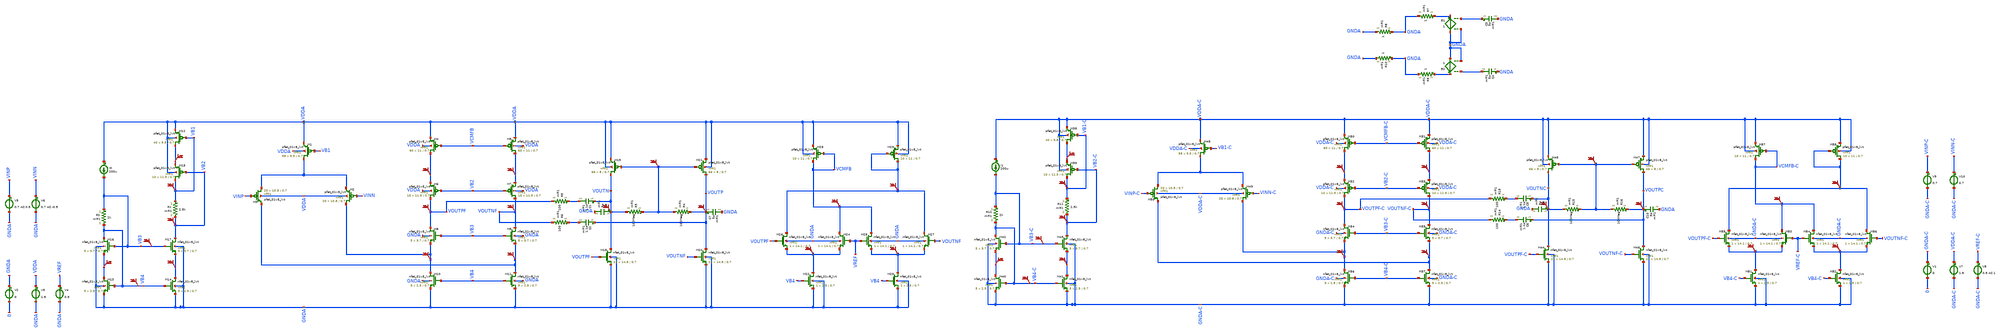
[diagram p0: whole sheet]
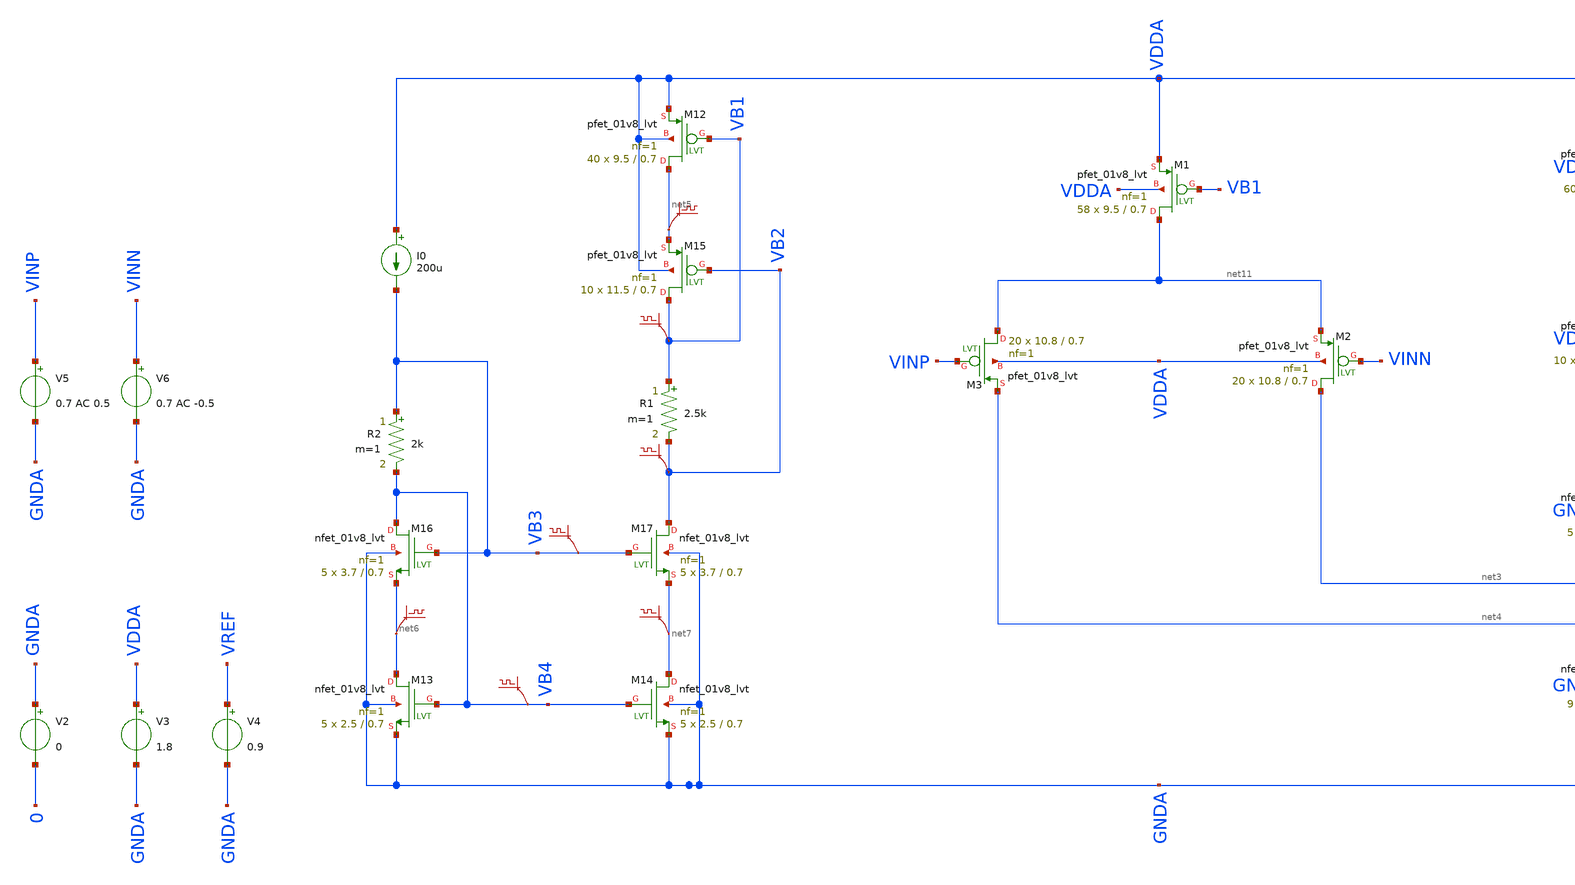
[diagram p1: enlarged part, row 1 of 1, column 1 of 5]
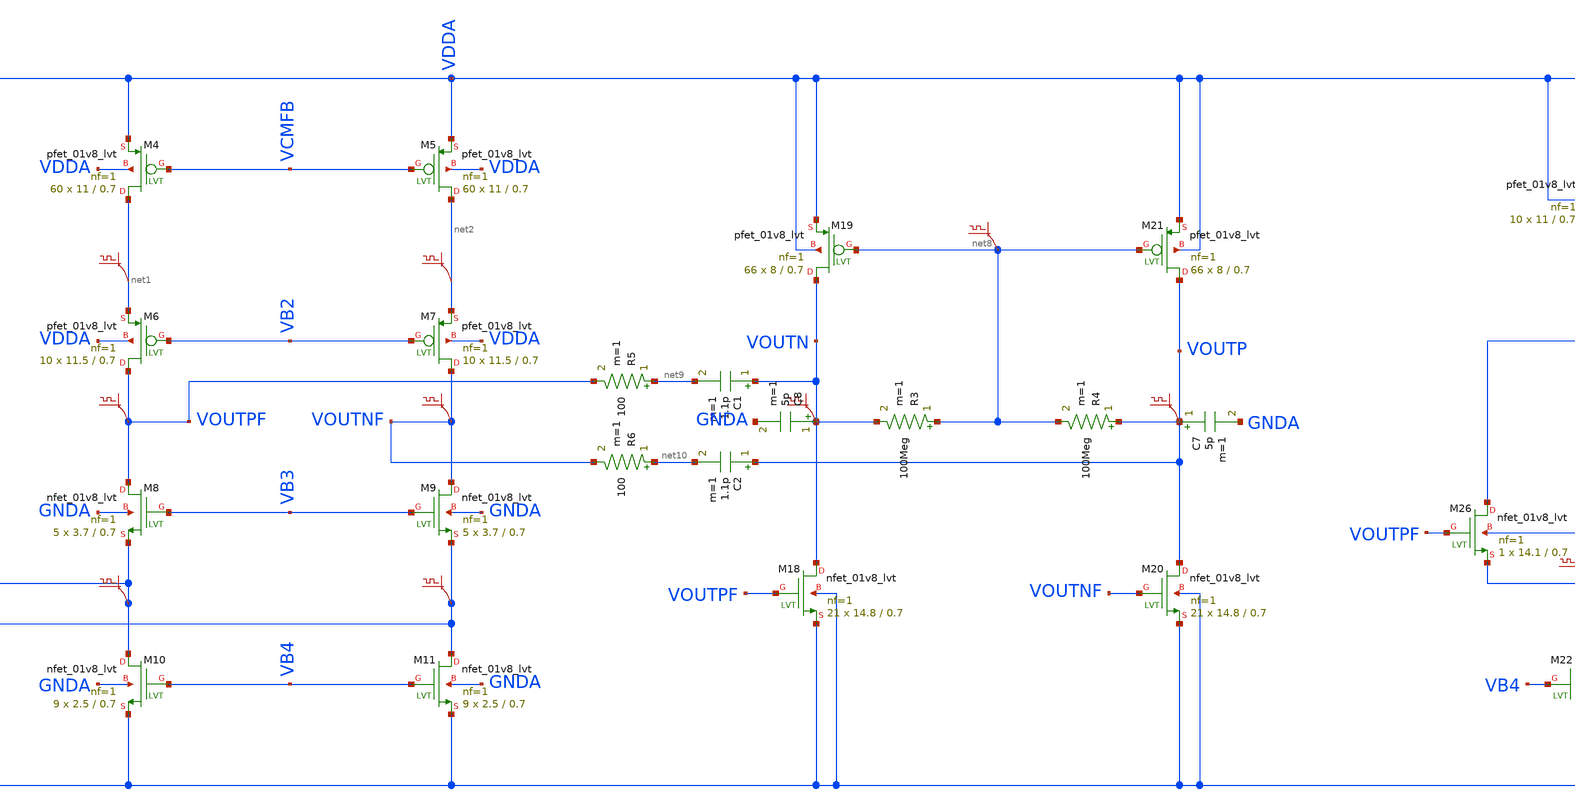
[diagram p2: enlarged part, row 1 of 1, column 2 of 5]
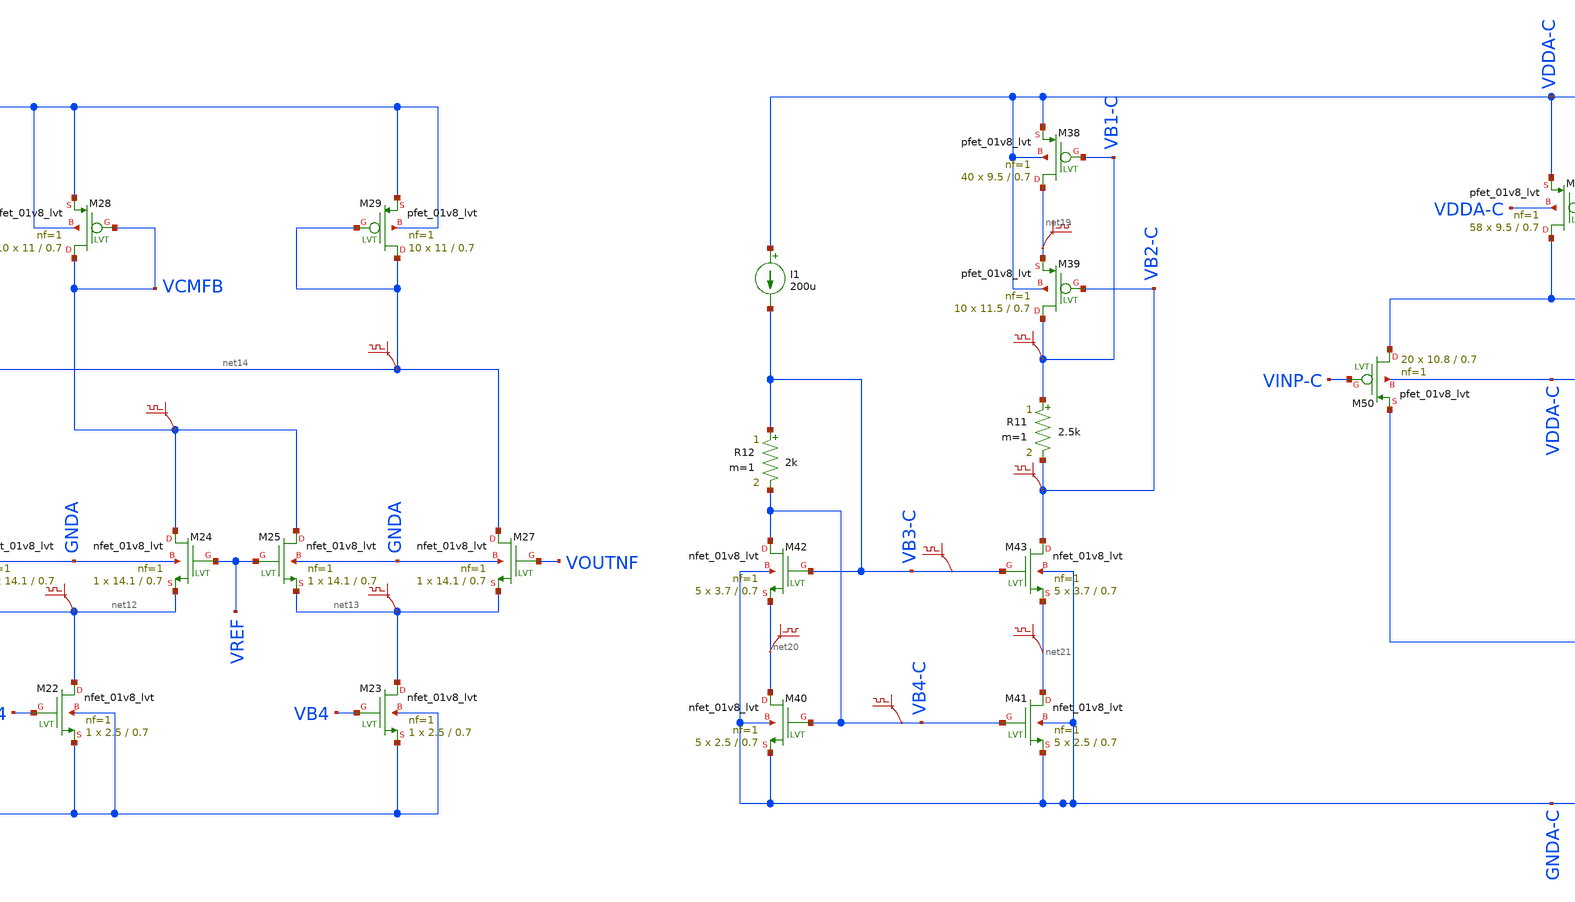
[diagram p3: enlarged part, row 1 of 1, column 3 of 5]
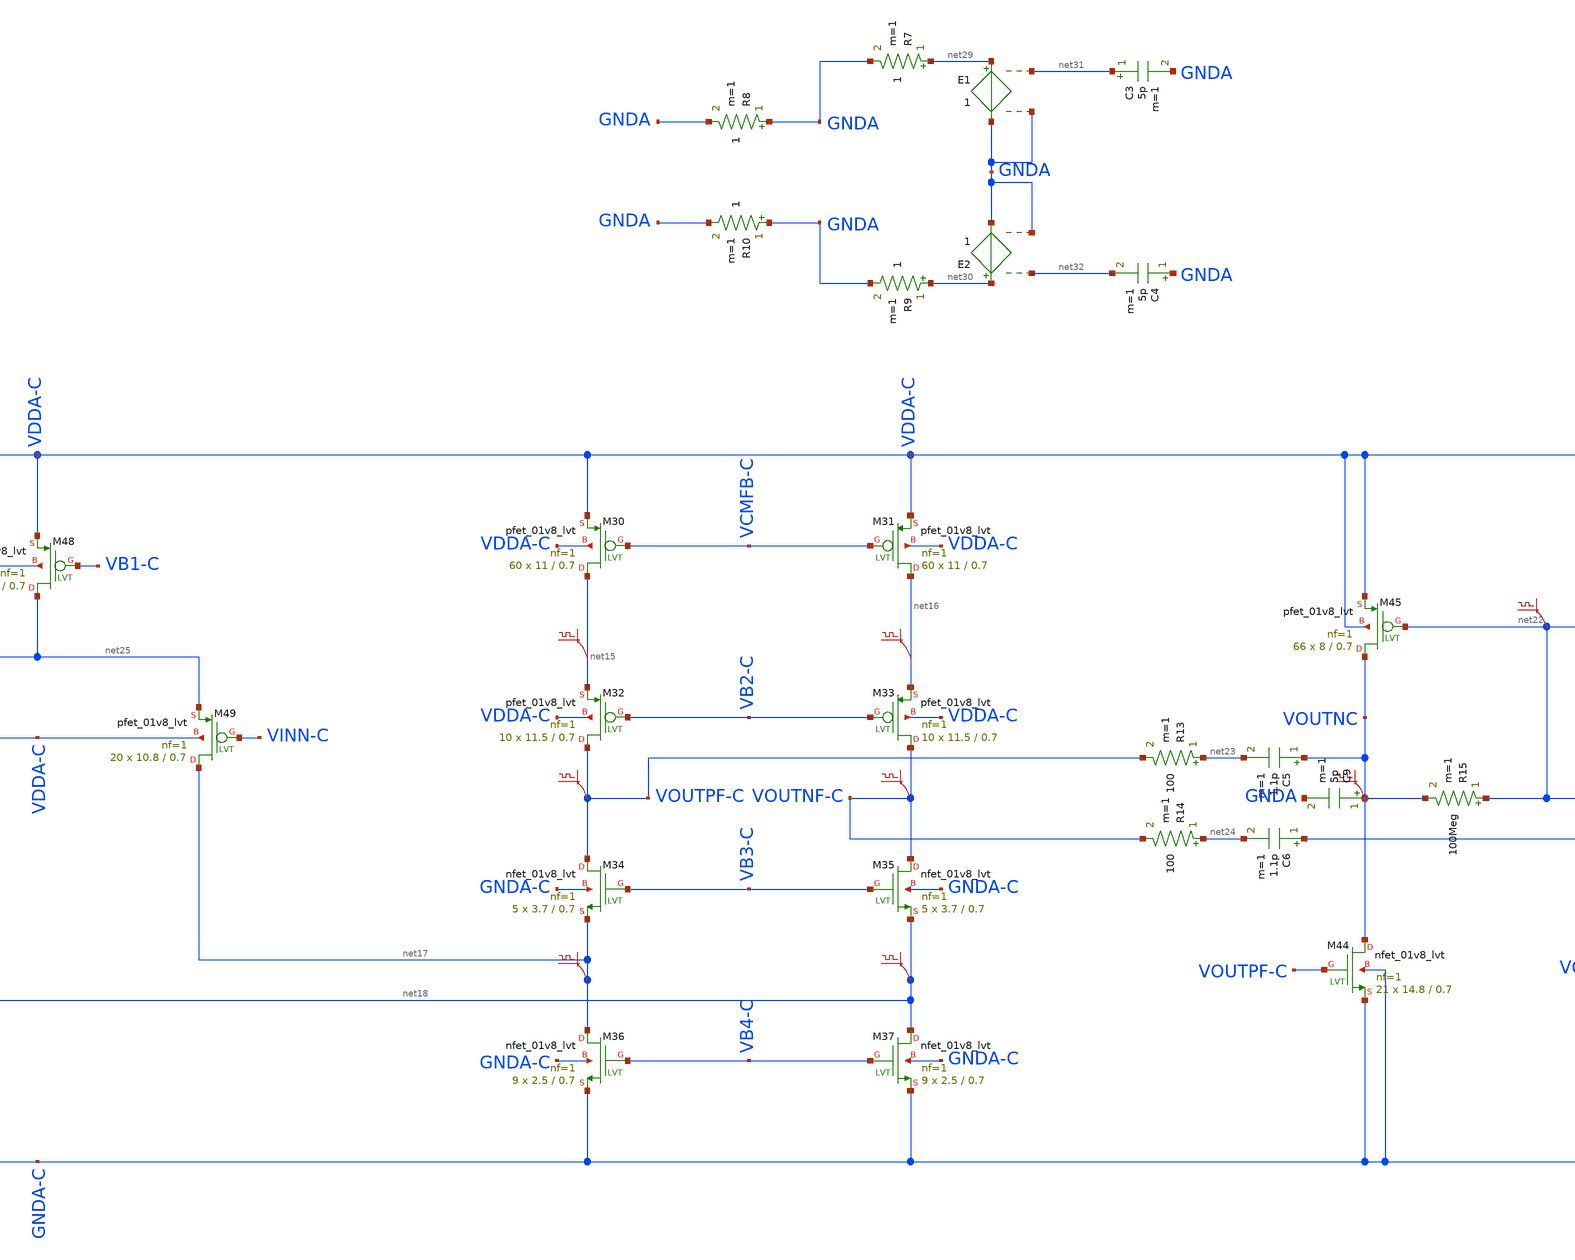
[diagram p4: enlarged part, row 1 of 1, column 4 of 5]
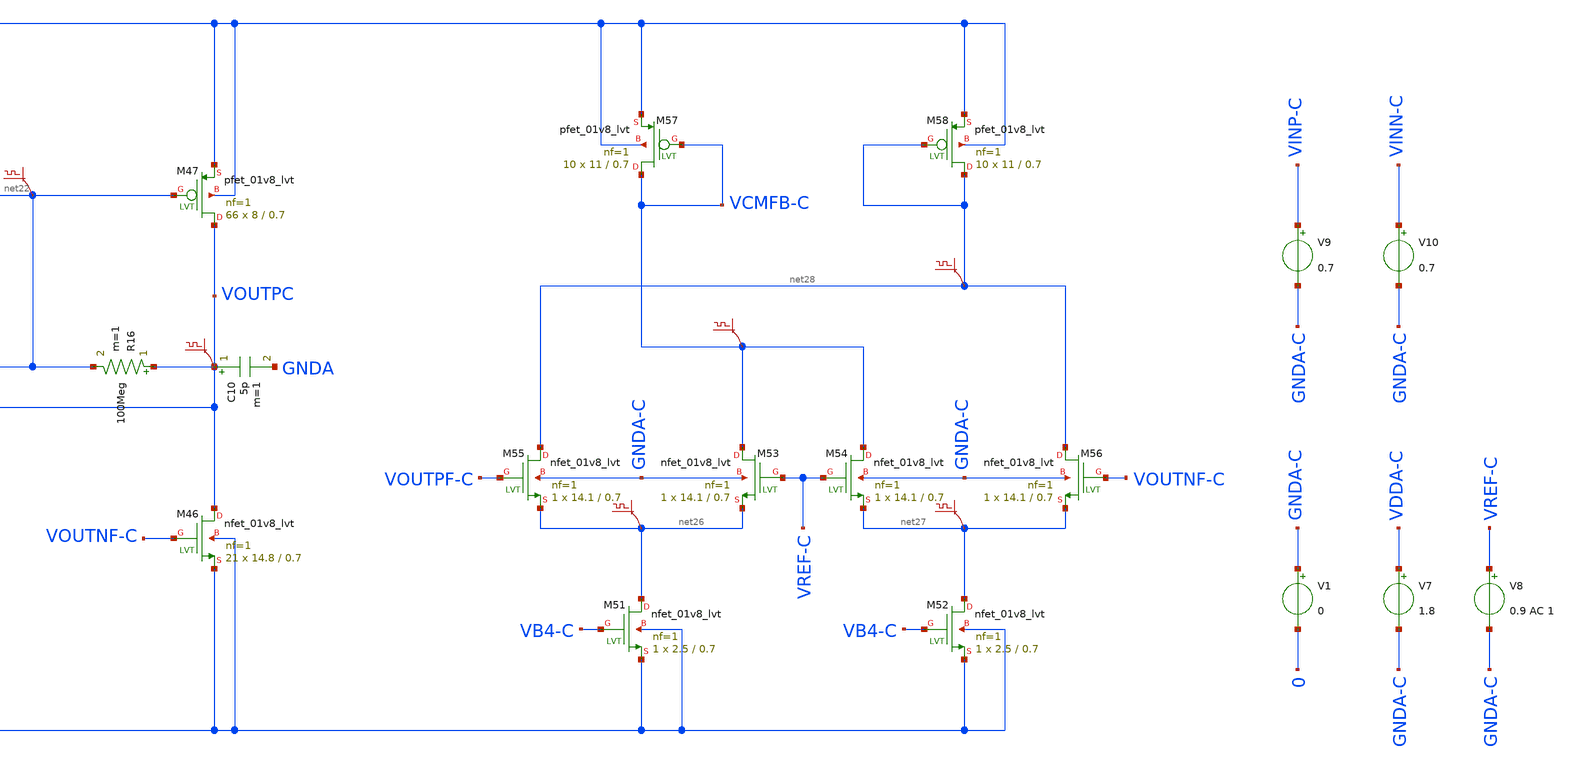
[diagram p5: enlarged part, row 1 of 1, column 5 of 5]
** sch_path: P_in_folded_cascode.sch
**.subckt P_in_folded_cascode
XM4 net1 VCMFB VDDA VDDA sky130_fd_pr__pfet_01v8_lvt L=0.7 W=11 nf=1 ad='int((nf+1)/2) * W/nf * 0.29'
+ as='int((nf+2)/2) * W/nf * 0.29' pd='2*int((nf+1)/2) * (W/nf + 0.29)' ps='2*int((nf+2)/2) * (W/nf + 0.29)'
+ nrd='0.29 / W' nrs='0.29 / W' sa=0 sb=0 sd=0 mult=60 m=60
XM5 net2 VCMFB VDDA VDDA sky130_fd_pr__pfet_01v8_lvt L=0.7 W=11 nf=1 ad='int((nf+1)/2) * W/nf * 0.29'
+ as='int((nf+2)/2) * W/nf * 0.29' pd='2*int((nf+1)/2) * (W/nf + 0.29)' ps='2*int((nf+2)/2) * (W/nf + 0.29)'
+ nrd='0.29 / W' nrs='0.29 / W' sa=0 sb=0 sd=0 mult=60 m=60
XM6 VOUTPF VB2 net1 VDDA sky130_fd_pr__pfet_01v8_lvt L=0.7 W=11.5 nf=1 ad='int((nf+1)/2) * W/nf * 0.29'
+ as='int((nf+2)/2) * W/nf * 0.29' pd='2*int((nf+1)/2) * (W/nf + 0.29)' ps='2*int((nf+2)/2) * (W/nf + 0.29)'
+ nrd='0.29 / W' nrs='0.29 / W' sa=0 sb=0 sd=0 mult=10 m=10
XM7 VOUTNF VB2 net2 VDDA sky130_fd_pr__pfet_01v8_lvt L=0.7 W=11.5 nf=1 ad='int((nf+1)/2) * W/nf * 0.29'
+ as='int((nf+2)/2) * W/nf * 0.29' pd='2*int((nf+1)/2) * (W/nf + 0.29)' ps='2*int((nf+2)/2) * (W/nf + 0.29)'
+ nrd='0.29 / W' nrs='0.29 / W' sa=0 sb=0 sd=0 mult=10 m=10
XM8 VOUTPF VB3 net3 GNDA sky130_fd_pr__nfet_01v8_lvt L=0.7 W=3.7 nf=1 ad='int((nf+1)/2) * W/nf * 0.29'
+ as='int((nf+2)/2) * W/nf * 0.29' pd='2*int((nf+1)/2) * (W/nf + 0.29)' ps='2*int((nf+2)/2) * (W/nf + 0.29)'
+ nrd='0.29 / W' nrs='0.29 / W' sa=0 sb=0 sd=0 mult=5 m=5
XM9 VOUTNF VB3 net4 GNDA sky130_fd_pr__nfet_01v8_lvt L=0.7 W=3.7 nf=1 ad='int((nf+1)/2) * W/nf * 0.29'
+ as='int((nf+2)/2) * W/nf * 0.29' pd='2*int((nf+1)/2) * (W/nf + 0.29)' ps='2*int((nf+2)/2) * (W/nf + 0.29)'
+ nrd='0.29 / W' nrs='0.29 / W' sa=0 sb=0 sd=0 mult=5 m=5
XM10 net3 VB4 GNDA GNDA sky130_fd_pr__nfet_01v8_lvt L=0.7 W=2.5 nf=1 ad='int((nf+1)/2) * W/nf * 0.29'
+ as='int((nf+2)/2) * W/nf * 0.29' pd='2*int((nf+1)/2) * (W/nf + 0.29)' ps='2*int((nf+2)/2) * (W/nf + 0.29)'
+ nrd='0.29 / W' nrs='0.29 / W' sa=0 sb=0 sd=0 mult=9 m=9
XM11 net4 VB4 GNDA GNDA sky130_fd_pr__nfet_01v8_lvt L=0.7 W=2.5 nf=1 ad='int((nf+1)/2) * W/nf * 0.29'
+ as='int((nf+2)/2) * W/nf * 0.29' pd='2*int((nf+1)/2) * (W/nf + 0.29)' ps='2*int((nf+2)/2) * (W/nf + 0.29)'
+ nrd='0.29 / W' nrs='0.29 / W' sa=0 sb=0 sd=0 mult=9 m=9
XM12 net5 VB1 VDDA VDDA sky130_fd_pr__pfet_01v8_lvt L=0.7 W=9.5 nf=1 ad='int((nf+1)/2) * W/nf * 0.29'
+ as='int((nf+2)/2) * W/nf * 0.29' pd='2*int((nf+1)/2) * (W/nf + 0.29)' ps='2*int((nf+2)/2) * (W/nf + 0.29)'
+ nrd='0.29 / W' nrs='0.29 / W' sa=0 sb=0 sd=0 mult=40 m=40
XM15 VB1 VB2 net5 VDDA sky130_fd_pr__pfet_01v8_lvt L=0.7 W=11.5 nf=1 ad='int((nf+1)/2) * W/nf * 0.29'
+ as='int((nf+2)/2) * W/nf * 0.29' pd='2*int((nf+1)/2) * (W/nf + 0.29)' ps='2*int((nf+2)/2) * (W/nf + 0.29)'
+ nrd='0.29 / W' nrs='0.29 / W' sa=0 sb=0 sd=0 mult=10 m=10
.save v(vb1)
.save v(net5)
R1 VB1 VB2 2.5k m=1
.save v(vb2)
XM13 net6 VB4 GNDA GNDA sky130_fd_pr__nfet_01v8_lvt L=0.7 W=2.5 nf=1 ad='int((nf+1)/2) * W/nf * 0.29'
+ as='int((nf+2)/2) * W/nf * 0.29' pd='2*int((nf+1)/2) * (W/nf + 0.29)' ps='2*int((nf+2)/2) * (W/nf + 0.29)'
+ nrd='0.29 / W' nrs='0.29 / W' sa=0 sb=0 sd=0 mult=5 m=5
XM14 net7 VB4 GNDA GNDA sky130_fd_pr__nfet_01v8_lvt L=0.7 W=2.5 nf=1 ad='int((nf+1)/2) * W/nf * 0.29'
+ as='int((nf+2)/2) * W/nf * 0.29' pd='2*int((nf+1)/2) * (W/nf + 0.29)' ps='2*int((nf+2)/2) * (W/nf + 0.29)'
+ nrd='0.29 / W' nrs='0.29 / W' sa=0 sb=0 sd=0 mult=5 m=5
XM16 VB4 VB3 net6 GNDA sky130_fd_pr__nfet_01v8_lvt L=0.7 W=3.7 nf=1 ad='int((nf+1)/2) * W/nf * 0.29'
+ as='int((nf+2)/2) * W/nf * 0.29' pd='2*int((nf+1)/2) * (W/nf + 0.29)' ps='2*int((nf+2)/2) * (W/nf + 0.29)'
+ nrd='0.29 / W' nrs='0.29 / W' sa=0 sb=0 sd=0 mult=5 m=5
XM17 VB2 VB3 net7 GNDA sky130_fd_pr__nfet_01v8_lvt L=0.7 W=3.7 nf=1 ad='int((nf+1)/2) * W/nf * 0.29'
+ as='int((nf+2)/2) * W/nf * 0.29' pd='2*int((nf+1)/2) * (W/nf + 0.29)' ps='2*int((nf+2)/2) * (W/nf + 0.29)'
+ nrd='0.29 / W' nrs='0.29 / W' sa=0 sb=0 sd=0 mult=5 m=5
.save v(net6)
.save v(net7)
.save v(vb4)
R2 VB3 VB4 2k m=1
I0 VDDA VB3 200u
XM18 VOUTN VOUTPF GNDA GNDA sky130_fd_pr__nfet_01v8_lvt L=0.7 W=14.8 nf=1 ad='int((nf+1)/2) * W/nf * 0.29'
+ as='int((nf+2)/2) * W/nf * 0.29' pd='2*int((nf+1)/2) * (W/nf + 0.29)' ps='2*int((nf+2)/2) * (W/nf + 0.29)'
+ nrd='0.29 / W' nrs='0.29 / W' sa=0 sb=0 sd=0 mult=21 m=21
XM19 VOUTN net8 VDDA VDDA sky130_fd_pr__pfet_01v8_lvt L=0.7 W=8 nf=1 ad='int((nf+1)/2) * W/nf * 0.29'
+ as='int((nf+2)/2) * W/nf * 0.29' pd='2*int((nf+1)/2) * (W/nf + 0.29)' ps='2*int((nf+2)/2) * (W/nf + 0.29)'
+ nrd='0.29 / W' nrs='0.29 / W' sa=0 sb=0 sd=0 mult=66 m=66
XM20 VOUTP VOUTNF GNDA GNDA sky130_fd_pr__nfet_01v8_lvt L=0.7 W=14.8 nf=1 ad='int((nf+1)/2) * W/nf * 0.29'
+ as='int((nf+2)/2) * W/nf * 0.29' pd='2*int((nf+1)/2) * (W/nf + 0.29)' ps='2*int((nf+2)/2) * (W/nf + 0.29)'
+ nrd='0.29 / W' nrs='0.29 / W' sa=0 sb=0 sd=0 mult=21 m=21
XM21 VOUTP net8 VDDA VDDA sky130_fd_pr__pfet_01v8_lvt L=0.7 W=8 nf=1 ad='int((nf+1)/2) * W/nf * 0.29'
+ as='int((nf+2)/2) * W/nf * 0.29' pd='2*int((nf+1)/2) * (W/nf + 0.29)' ps='2*int((nf+2)/2) * (W/nf + 0.29)'
+ nrd='0.29 / W' nrs='0.29 / W' sa=0 sb=0 sd=0 mult=66 m=66
R5 net9 VOUTPF 100 m=1
R6 net10 VOUTNF 100 m=1
C1 VOUTN net9 1.1p m=1
C2 VOUTP net10 1.1p m=1
V2 GNDA 0 0
V3 VDDA GNDA 1.8
V4 VREF GNDA 0.9
V5 VINP GNDA 0.7 AC 0.5
V6 VINN GNDA 0.7 AC -0.5
.save v(net1)
.save v(net2)
.save v(voutpf)
.save v(voutnf)
.save v(net3)
.save v(net4)
.save v(voutn)
.save v(voutp)
.save v(vb3)
XM1 net11 VB1 VDDA VDDA sky130_fd_pr__pfet_01v8_lvt L=0.7 W=9.5 nf=1 ad='int((nf+1)/2) * W/nf * 0.29'
+ as='int((nf+2)/2) * W/nf * 0.29' pd='2*int((nf+1)/2) * (W/nf + 0.29)' ps='2*int((nf+2)/2) * (W/nf + 0.29)'
+ nrd='0.29 / W' nrs='0.29 / W' sa=0 sb=0 sd=0 mult=58 m=58
XM2 net3 VINN net11 VDDA sky130_fd_pr__pfet_01v8_lvt L=0.7 W=10.8 nf=1 ad='int((nf+1)/2) * W/nf * 0.29'
+ as='int((nf+2)/2) * W/nf * 0.29' pd='2*int((nf+1)/2) * (W/nf + 0.29)' ps='2*int((nf+2)/2) * (W/nf + 0.29)'
+ nrd='0.29 / W' nrs='0.29 / W' sa=0 sb=0 sd=0 mult=20 m=20
XM3 net11 VINP net4 VDDA sky130_fd_pr__pfet_01v8_lvt L=0.7 W=10.8 nf=1 ad='int((nf+1)/2) * W/nf * 0.29'
+ as='int((nf+2)/2) * W/nf * 0.29' pd='2*int((nf+1)/2) * (W/nf + 0.29)' ps='2*int((nf+2)/2) * (W/nf + 0.29)'
+ nrd='0.29 / W' nrs='0.29 / W' sa=0 sb=0 sd=0 mult=20 m=20
R3 net8 VOUTN 100Meg m=1
R4 VOUTP net8 100Meg m=1
XM22 net12 VB4 GNDA GNDA sky130_fd_pr__nfet_01v8_lvt L=0.7 W=2.5 nf=1 ad='int((nf+1)/2) * W/nf * 0.29'
+ as='int((nf+2)/2) * W/nf * 0.29' pd='2*int((nf+1)/2) * (W/nf + 0.29)' ps='2*int((nf+2)/2) * (W/nf + 0.29)'
+ nrd='0.29 / W' nrs='0.29 / W' sa=0 sb=0 sd=0 mult=1 m=1
XM23 net13 VB4 GNDA GNDA sky130_fd_pr__nfet_01v8_lvt L=0.7 W=2.5 nf=1 ad='int((nf+1)/2) * W/nf * 0.29'
+ as='int((nf+2)/2) * W/nf * 0.29' pd='2*int((nf+1)/2) * (W/nf + 0.29)' ps='2*int((nf+2)/2) * (W/nf + 0.29)'
+ nrd='0.29 / W' nrs='0.29 / W' sa=0 sb=0 sd=0 mult=1 m=1
XM24 VCMFB VREF net12 GNDA sky130_fd_pr__nfet_01v8_lvt L=0.7 W=14.1 nf=1 ad='int((nf+1)/2) * W/nf * 0.29'
+ as='int((nf+2)/2) * W/nf * 0.29' pd='2*int((nf+1)/2) * (W/nf + 0.29)' ps='2*int((nf+2)/2) * (W/nf + 0.29)'
+ nrd='0.29 / W' nrs='0.29 / W' sa=0 sb=0 sd=0 mult=1 m=1
XM25 VCMFB VREF net13 GNDA sky130_fd_pr__nfet_01v8_lvt L=0.7 W=14.1 nf=1 ad='int((nf+1)/2) * W/nf * 0.29'
+ as='int((nf+2)/2) * W/nf * 0.29' pd='2*int((nf+1)/2) * (W/nf + 0.29)' ps='2*int((nf+2)/2) * (W/nf + 0.29)'
+ nrd='0.29 / W' nrs='0.29 / W' sa=0 sb=0 sd=0 mult=1 m=1
XM26 net14 VOUTPF net12 GNDA sky130_fd_pr__nfet_01v8_lvt L=0.7 W=14.1 nf=1 ad='int((nf+1)/2) * W/nf * 0.29'
+ as='int((nf+2)/2) * W/nf * 0.29' pd='2*int((nf+1)/2) * (W/nf + 0.29)' ps='2*int((nf+2)/2) * (W/nf + 0.29)'
+ nrd='0.29 / W' nrs='0.29 / W' sa=0 sb=0 sd=0 mult=1 m=1
XM27 net14 VOUTNF net13 GNDA sky130_fd_pr__nfet_01v8_lvt L=0.7 W=14.1 nf=1 ad='int((nf+1)/2) * W/nf * 0.29'
+ as='int((nf+2)/2) * W/nf * 0.29' pd='2*int((nf+1)/2) * (W/nf + 0.29)' ps='2*int((nf+2)/2) * (W/nf + 0.29)'
+ nrd='0.29 / W' nrs='0.29 / W' sa=0 sb=0 sd=0 mult=1 m=1
XM28 VCMFB VCMFB VDDA VDDA sky130_fd_pr__pfet_01v8_lvt L=0.7 W=11 nf=1 ad='int((nf+1)/2) * W/nf * 0.29'
+ as='int((nf+2)/2) * W/nf * 0.29' pd='2*int((nf+1)/2) * (W/nf + 0.29)' ps='2*int((nf+2)/2) * (W/nf + 0.29)'
+ nrd='0.29 / W' nrs='0.29 / W' sa=0 sb=0 sd=0 mult=10 m=10
XM29 net14 net14 VDDA VDDA sky130_fd_pr__pfet_01v8_lvt L=0.7 W=11 nf=1 ad='int((nf+1)/2) * W/nf * 0.29'
+ as='int((nf+2)/2) * W/nf * 0.29' pd='2*int((nf+1)/2) * (W/nf + 0.29)' ps='2*int((nf+2)/2) * (W/nf + 0.29)'
+ nrd='0.29 / W' nrs='0.29 / W' sa=0 sb=0 sd=0 mult=10 m=10
.save v(net12)
.save v(net13)
.save v(vcmfb)
.save v(net14)
.save v(net8)
XM30 net15 VCMFB-C VDDA-C VDDA-C sky130_fd_pr__pfet_01v8_lvt L=0.7 W=11 nf=1 ad='int((nf+1)/2) * W/nf * 0.29'
+ as='int((nf+2)/2) * W/nf * 0.29' pd='2*int((nf+1)/2) * (W/nf + 0.29)' ps='2*int((nf+2)/2) * (W/nf + 0.29)'
+ nrd='0.29 / W' nrs='0.29 / W' sa=0 sb=0 sd=0 mult=60 m=60
XM31 net16 VCMFB-C VDDA-C VDDA-C sky130_fd_pr__pfet_01v8_lvt L=0.7 W=11 nf=1 ad='int((nf+1)/2) * W/nf * 0.29'
+ as='int((nf+2)/2) * W/nf * 0.29' pd='2*int((nf+1)/2) * (W/nf + 0.29)' ps='2*int((nf+2)/2) * (W/nf + 0.29)'
+ nrd='0.29 / W' nrs='0.29 / W' sa=0 sb=0 sd=0 mult=60 m=60
XM32 VOUTPF-C VB2-C net15 VDDA-C sky130_fd_pr__pfet_01v8_lvt L=0.7 W=11.5 nf=1 ad='int((nf+1)/2) * W/nf * 0.29'
+ as='int((nf+2)/2) * W/nf * 0.29' pd='2*int((nf+1)/2) * (W/nf + 0.29)' ps='2*int((nf+2)/2) * (W/nf + 0.29)'
+ nrd='0.29 / W' nrs='0.29 / W' sa=0 sb=0 sd=0 mult=10 m=10
XM33 VOUTNF-C VB2-C net16 VDDA-C sky130_fd_pr__pfet_01v8_lvt L=0.7 W=11.5 nf=1 ad='int((nf+1)/2) * W/nf * 0.29'
+ as='int((nf+2)/2) * W/nf * 0.29' pd='2*int((nf+1)/2) * (W/nf + 0.29)' ps='2*int((nf+2)/2) * (W/nf + 0.29)'
+ nrd='0.29 / W' nrs='0.29 / W' sa=0 sb=0 sd=0 mult=10 m=10
XM34 VOUTPF-C VB3-C net17 GNDA-C sky130_fd_pr__nfet_01v8_lvt L=0.7 W=3.7 nf=1 ad='int((nf+1)/2) * W/nf * 0.29'
+ as='int((nf+2)/2) * W/nf * 0.29' pd='2*int((nf+1)/2) * (W/nf + 0.29)' ps='2*int((nf+2)/2) * (W/nf + 0.29)'
+ nrd='0.29 / W' nrs='0.29 / W' sa=0 sb=0 sd=0 mult=5 m=5
XM35 VOUTNF-C VB3-C net18 GNDA-C sky130_fd_pr__nfet_01v8_lvt L=0.7 W=3.7 nf=1 ad='int((nf+1)/2) * W/nf * 0.29'
+ as='int((nf+2)/2) * W/nf * 0.29' pd='2*int((nf+1)/2) * (W/nf + 0.29)' ps='2*int((nf+2)/2) * (W/nf + 0.29)'
+ nrd='0.29 / W' nrs='0.29 / W' sa=0 sb=0 sd=0 mult=5 m=5
XM36 net17 VB4-C GNDA-C GNDA-C sky130_fd_pr__nfet_01v8_lvt L=0.7 W=2.5 nf=1 ad='int((nf+1)/2) * W/nf * 0.29'
+ as='int((nf+2)/2) * W/nf * 0.29' pd='2*int((nf+1)/2) * (W/nf + 0.29)' ps='2*int((nf+2)/2) * (W/nf + 0.29)'
+ nrd='0.29 / W' nrs='0.29 / W' sa=0 sb=0 sd=0 mult=9 m=9
XM37 net18 VB4-C GNDA-C GNDA-C sky130_fd_pr__nfet_01v8_lvt L=0.7 W=2.5 nf=1 ad='int((nf+1)/2) * W/nf * 0.29'
+ as='int((nf+2)/2) * W/nf * 0.29' pd='2*int((nf+1)/2) * (W/nf + 0.29)' ps='2*int((nf+2)/2) * (W/nf + 0.29)'
+ nrd='0.29 / W' nrs='0.29 / W' sa=0 sb=0 sd=0 mult=9 m=9
XM38 net19 VB1-C VDDA-C VDDA-C sky130_fd_pr__pfet_01v8_lvt L=0.7 W=9.5 nf=1 ad='int((nf+1)/2) * W/nf * 0.29'
+ as='int((nf+2)/2) * W/nf * 0.29' pd='2*int((nf+1)/2) * (W/nf + 0.29)' ps='2*int((nf+2)/2) * (W/nf + 0.29)'
+ nrd='0.29 / W' nrs='0.29 / W' sa=0 sb=0 sd=0 mult=40 m=40
XM39 VB1-C VB2-C net19 VDDA-C sky130_fd_pr__pfet_01v8_lvt L=0.7 W=11.5 nf=1 ad='int((nf+1)/2) * W/nf * 0.29'
+ as='int((nf+2)/2) * W/nf * 0.29' pd='2*int((nf+1)/2) * (W/nf + 0.29)' ps='2*int((nf+2)/2) * (W/nf + 0.29)'
+ nrd='0.29 / W' nrs='0.29 / W' sa=0 sb=0 sd=0 mult=10 m=10
.save v(vb1-c)
.save v(net19)
R11 VB1-C VB2-C 2.5k m=1
.save v(vb2-c)
XM40 net20 VB4-C GNDA-C GNDA-C sky130_fd_pr__nfet_01v8_lvt L=0.7 W=2.5 nf=1 ad='int((nf+1)/2) * W/nf * 0.29'
+ as='int((nf+2)/2) * W/nf * 0.29' pd='2*int((nf+1)/2) * (W/nf + 0.29)' ps='2*int((nf+2)/2) * (W/nf + 0.29)'
+ nrd='0.29 / W' nrs='0.29 / W' sa=0 sb=0 sd=0 mult=5 m=5
XM41 net21 VB4-C GNDA-C GNDA-C sky130_fd_pr__nfet_01v8_lvt L=0.7 W=2.5 nf=1 ad='int((nf+1)/2) * W/nf * 0.29'
+ as='int((nf+2)/2) * W/nf * 0.29' pd='2*int((nf+1)/2) * (W/nf + 0.29)' ps='2*int((nf+2)/2) * (W/nf + 0.29)'
+ nrd='0.29 / W' nrs='0.29 / W' sa=0 sb=0 sd=0 mult=5 m=5
XM42 VB4-C VB3-C net20 GNDA-C sky130_fd_pr__nfet_01v8_lvt L=0.7 W=3.7 nf=1 ad='int((nf+1)/2) * W/nf * 0.29'
+ as='int((nf+2)/2) * W/nf * 0.29' pd='2*int((nf+1)/2) * (W/nf + 0.29)' ps='2*int((nf+2)/2) * (W/nf + 0.29)'
+ nrd='0.29 / W' nrs='0.29 / W' sa=0 sb=0 sd=0 mult=5 m=5
XM43 VB2-C VB3-C net21 GNDA-C sky130_fd_pr__nfet_01v8_lvt L=0.7 W=3.7 nf=1 ad='int((nf+1)/2) * W/nf * 0.29'
+ as='int((nf+2)/2) * W/nf * 0.29' pd='2*int((nf+1)/2) * (W/nf + 0.29)' ps='2*int((nf+2)/2) * (W/nf + 0.29)'
+ nrd='0.29 / W' nrs='0.29 / W' sa=0 sb=0 sd=0 mult=5 m=5
.save v(net20)
.save v(net21)
.save v(vb4-c)
R12 VB3-C VB4-C 2k m=1
I1 VDDA-C VB3-C 200u
XM44 VOUTNC VOUTPF-C GNDA-C GNDA-C sky130_fd_pr__nfet_01v8_lvt L=0.7 W=14.8 nf=1 ad='int((nf+1)/2) * W/nf * 0.29'
+ as='int((nf+2)/2) * W/nf * 0.29' pd='2*int((nf+1)/2) * (W/nf + 0.29)' ps='2*int((nf+2)/2) * (W/nf + 0.29)'
+ nrd='0.29 / W' nrs='0.29 / W' sa=0 sb=0 sd=0 mult=21 m=21
XM45 VOUTNC net22 VDDA-C VDDA-C sky130_fd_pr__pfet_01v8_lvt L=0.7 W=8 nf=1 ad='int((nf+1)/2) * W/nf * 0.29'
+ as='int((nf+2)/2) * W/nf * 0.29' pd='2*int((nf+1)/2) * (W/nf + 0.29)' ps='2*int((nf+2)/2) * (W/nf + 0.29)'
+ nrd='0.29 / W' nrs='0.29 / W' sa=0 sb=0 sd=0 mult=66 m=66
XM46 VOUTPC VOUTNF-C GNDA-C GNDA-C sky130_fd_pr__nfet_01v8_lvt L=0.7 W=14.8 nf=1 ad='int((nf+1)/2) * W/nf * 0.29'
+ as='int((nf+2)/2) * W/nf * 0.29' pd='2*int((nf+1)/2) * (W/nf + 0.29)' ps='2*int((nf+2)/2) * (W/nf + 0.29)'
+ nrd='0.29 / W' nrs='0.29 / W' sa=0 sb=0 sd=0 mult=21 m=21
XM47 VOUTPC net22 VDDA-C VDDA-C sky130_fd_pr__pfet_01v8_lvt L=0.7 W=8 nf=1 ad='int((nf+1)/2) * W/nf * 0.29'
+ as='int((nf+2)/2) * W/nf * 0.29' pd='2*int((nf+1)/2) * (W/nf + 0.29)' ps='2*int((nf+2)/2) * (W/nf + 0.29)'
+ nrd='0.29 / W' nrs='0.29 / W' sa=0 sb=0 sd=0 mult=66 m=66
R13 net23 VOUTPF-C 100 m=1
R14 net24 VOUTNF-C 100 m=1
C5 VOUTNC net23 1.1p m=1
C6 VOUTPC net24 1.1p m=1
.save v(net15)
.save v(net16)
.save v(voutpf-c)
.save v(voutnf-c)
.save v(net17)
.save v(net18)
.save v(voutnc)
.save v(voutpc)
.save v(vb3-c)
XM48 net25 VB1-C VDDA-C VDDA-C sky130_fd_pr__pfet_01v8_lvt L=0.7 W=9.5 nf=1 ad='int((nf+1)/2) * W/nf * 0.29'
+ as='int((nf+2)/2) * W/nf * 0.29' pd='2*int((nf+1)/2) * (W/nf + 0.29)' ps='2*int((nf+2)/2) * (W/nf + 0.29)'
+ nrd='0.29 / W' nrs='0.29 / W' sa=0 sb=0 sd=0 mult=58 m=58
XM49 net17 VINN-C net25 VDDA-C sky130_fd_pr__pfet_01v8_lvt L=0.7 W=10.8 nf=1 ad='int((nf+1)/2) * W/nf * 0.29'
+ as='int((nf+2)/2) * W/nf * 0.29' pd='2*int((nf+1)/2) * (W/nf + 0.29)' ps='2*int((nf+2)/2) * (W/nf + 0.29)'
+ nrd='0.29 / W' nrs='0.29 / W' sa=0 sb=0 sd=0 mult=20 m=20
XM50 net25 VINP-C net18 VDDA-C sky130_fd_pr__pfet_01v8_lvt L=0.7 W=10.8 nf=1 ad='int((nf+1)/2) * W/nf * 0.29'
+ as='int((nf+2)/2) * W/nf * 0.29' pd='2*int((nf+1)/2) * (W/nf + 0.29)' ps='2*int((nf+2)/2) * (W/nf + 0.29)'
+ nrd='0.29 / W' nrs='0.29 / W' sa=0 sb=0 sd=0 mult=20 m=20
R15 net22 VOUTNC 100Meg m=1
R16 VOUTPC net22 100Meg m=1
XM51 net26 VB4-C GNDA-C GNDA-C sky130_fd_pr__nfet_01v8_lvt L=0.7 W=2.5 nf=1 ad='int((nf+1)/2) * W/nf * 0.29'
+ as='int((nf+2)/2) * W/nf * 0.29' pd='2*int((nf+1)/2) * (W/nf + 0.29)' ps='2*int((nf+2)/2) * (W/nf + 0.29)'
+ nrd='0.29 / W' nrs='0.29 / W' sa=0 sb=0 sd=0 mult=1 m=1
XM52 net27 VB4-C GNDA-C GNDA-C sky130_fd_pr__nfet_01v8_lvt L=0.7 W=2.5 nf=1 ad='int((nf+1)/2) * W/nf * 0.29'
+ as='int((nf+2)/2) * W/nf * 0.29' pd='2*int((nf+1)/2) * (W/nf + 0.29)' ps='2*int((nf+2)/2) * (W/nf + 0.29)'
+ nrd='0.29 / W' nrs='0.29 / W' sa=0 sb=0 sd=0 mult=1 m=1
XM53 VCMFB-C VREF-C net26 GNDA-C sky130_fd_pr__nfet_01v8_lvt L=0.7 W=14.1 nf=1 ad='int((nf+1)/2) * W/nf * 0.29'
+ as='int((nf+2)/2) * W/nf * 0.29' pd='2*int((nf+1)/2) * (W/nf + 0.29)' ps='2*int((nf+2)/2) * (W/nf + 0.29)'
+ nrd='0.29 / W' nrs='0.29 / W' sa=0 sb=0 sd=0 mult=1 m=1
XM54 VCMFB-C VREF-C net27 GNDA-C sky130_fd_pr__nfet_01v8_lvt L=0.7 W=14.1 nf=1 ad='int((nf+1)/2) * W/nf * 0.29'
+ as='int((nf+2)/2) * W/nf * 0.29' pd='2*int((nf+1)/2) * (W/nf + 0.29)' ps='2*int((nf+2)/2) * (W/nf + 0.29)'
+ nrd='0.29 / W' nrs='0.29 / W' sa=0 sb=0 sd=0 mult=1 m=1
XM55 net28 VOUTPF-C net26 GNDA-C sky130_fd_pr__nfet_01v8_lvt L=0.7 W=14.1 nf=1 ad='int((nf+1)/2) * W/nf * 0.29'
+ as='int((nf+2)/2) * W/nf * 0.29' pd='2*int((nf+1)/2) * (W/nf + 0.29)' ps='2*int((nf+2)/2) * (W/nf + 0.29)'
+ nrd='0.29 / W' nrs='0.29 / W' sa=0 sb=0 sd=0 mult=1 m=1
XM56 net28 VOUTNF-C net27 GNDA-C sky130_fd_pr__nfet_01v8_lvt L=0.7 W=14.1 nf=1 ad='int((nf+1)/2) * W/nf * 0.29'
+ as='int((nf+2)/2) * W/nf * 0.29' pd='2*int((nf+1)/2) * (W/nf + 0.29)' ps='2*int((nf+2)/2) * (W/nf + 0.29)'
+ nrd='0.29 / W' nrs='0.29 / W' sa=0 sb=0 sd=0 mult=1 m=1
XM57 VCMFB-C VCMFB-C VDDA-C VDDA-C sky130_fd_pr__pfet_01v8_lvt L=0.7 W=11 nf=1 ad='int((nf+1)/2) * W/nf * 0.29'
+ as='int((nf+2)/2) * W/nf * 0.29' pd='2*int((nf+1)/2) * (W/nf + 0.29)' ps='2*int((nf+2)/2) * (W/nf + 0.29)'
+ nrd='0.29 / W' nrs='0.29 / W' sa=0 sb=0 sd=0 mult=10 m=10
XM58 net28 net28 VDDA-C VDDA-C sky130_fd_pr__pfet_01v8_lvt L=0.7 W=11 nf=1 ad='int((nf+1)/2) * W/nf * 0.29'
+ as='int((nf+2)/2) * W/nf * 0.29' pd='2*int((nf+1)/2) * (W/nf + 0.29)' ps='2*int((nf+2)/2) * (W/nf + 0.29)'
+ nrd='0.29 / W' nrs='0.29 / W' sa=0 sb=0 sd=0 mult=10 m=10
.save v(net26)
.save v(net27)
.save v(vcmfb-c)
.save v(net28)
.save v(net22)
V1 GNDA-C 0 0
V7 VDDA-C GNDA-C 1.8
V8 VREF-C GNDA-C 0.9 AC 1
V9 VINP-C GNDA-C 0.7
V10 VINN-C GNDA-C 0.7
C7 VOUTP GNDA 5p m=1
C8 VOUTN GNDA 5p m=1
C9 VOUTNC GNDA 5p m=1
C10 VOUTPC GNDA 5p m=1
C3 net31 GNDA 5p m=1
C4 GNDA net32 5p m=1
R7 net29 GNDA 1 m=1
R8 GNDA GNDA 1 m=1
R9 net30 GNDA 1 m=1
R10 GNDA GNDA 1 m=1
E1 net29 GNDA net31 GNDA 1
E2 net30 GNDA net32 GNDA 1
**** begin user architecture code

** opencircuitdesign pdks install
.lib $::SKYWATER_MODELS/sky130.lib.spice ff



.control
save all
save @m.xm1.msky130_fd_pr__pfet_01v8_lvt[vth]
save @m.xm1.msky130_fd_pr__pfet_01v8_lvt[id]
save @m.xm1.msky130_fd_pr__pfet_01v8_lvt[gds]
save @m.xm1.msky130_fd_pr__pfet_01v8_lvt[gm]
save @m.xm1.msky130_fd_pr__pfet_01v8_lvt[vdsat]
save @m.xm1.msky130_fd_pr__pfet_01v8_lvt[cgg]
save @m.xm1.msky130_fd_pr__pfet_01v8_lvt[cgd]

save @m.xm3.msky130_fd_pr__pfet_01v8_lvt[vth]
save @m.xm3.msky130_fd_pr__pfet_01v8_lvt[id]
save @m.xm3.msky130_fd_pr__pfet_01v8_lvt[gds]
save @m.xm3.msky130_fd_pr__pfet_01v8_lvt[gm]
save @m.xm3.msky130_fd_pr__pfet_01v8_lvt[vdsat]
save @m.xm3.msky130_fd_pr__pfet_01v8_lvt[cgg]
save @m.xm3.msky130_fd_pr__pfet_01v8_lvt[cgd]

save @m.xm8.msky130_fd_pr__nfet_01v8_lvt[vth]
save @m.xm8.msky130_fd_pr__nfet_01v8_lvt[id]
save @m.xm8.msky130_fd_pr__nfet_01v8_lvt[gds]
save @m.xm8.msky130_fd_pr__nfet_01v8_lvt[gm]
save @m.xm8.msky130_fd_pr__nfet_01v8_lvt[vdsat]
save @m.xm8.msky130_fd_pr__nfet_01v8_lvt[cgg]
save @m.xm8.msky130_fd_pr__nfet_01v8_lvt[cgd]

save @m.xm9.msky130_fd_pr__nfet_01v8_lvt[vth]
save @m.xm9.msky130_fd_pr__nfet_01v8_lvt[id]
save @m.xm9.msky130_fd_pr__nfet_01v8_lvt[gds]
save @m.xm9.msky130_fd_pr__nfet_01v8_lvt[gm]
save @m.xm9.msky130_fd_pr__nfet_01v8_lvt[vdsat]
save @m.xm9.msky130_fd_pr__nfet_01v8_lvt[cgg]
save @m.xm9.msky130_fd_pr__nfet_01v8_lvt[cgd]

save @m.xm10.msky130_fd_pr__nfet_01v8_lvt[vth]
save @m.xm10.msky130_fd_pr__nfet_01v8_lvt[id]
save @m.xm10.msky130_fd_pr__nfet_01v8_lvt[gds]
save @m.xm10.msky130_fd_pr__nfet_01v8_lvt[gm]
save @m.xm10.msky130_fd_pr__nfet_01v8_lvt[vdsat]
save @m.xm10.msky130_fd_pr__nfet_01v8_lvt[cgg]
save @m.xm10.msky130_fd_pr__nfet_01v8_lvt[cgd]

save @m.xm11.msky130_fd_pr__nfet_01v8_lvt[vth]
save @m.xm11.msky130_fd_pr__nfet_01v8_lvt[id]
save @m.xm11.msky130_fd_pr__nfet_01v8_lvt[gds]
save @m.xm11.msky130_fd_pr__nfet_01v8_lvt[gm]
save @m.xm11.msky130_fd_pr__nfet_01v8_lvt[vdsat]
save @m.xm11.msky130_fd_pr__nfet_01v8_lvt[cgg]
save @m.xm11.msky130_fd_pr__nfet_01v8_lvt[cgd]

save @m.xm13.msky130_fd_pr__nfet_01v8_lvt[vth]
save @m.xm13.msky130_fd_pr__nfet_01v8_lvt[id]
save @m.xm13.msky130_fd_pr__nfet_01v8_lvt[gds]
save @m.xm13.msky130_fd_pr__nfet_01v8_lvt[gm]
save @m.xm13.msky130_fd_pr__nfet_01v8_lvt[vdsat]
save @m.xm13.msky130_fd_pr__nfet_01v8_lvt[cgg]
save @m.xm13.msky130_fd_pr__nfet_01v8_lvt[cgd]

save @m.xm14.msky130_fd_pr__nfet_01v8_lvt[vth]
save @m.xm14.msky130_fd_pr__nfet_01v8_lvt[id]
save @m.xm14.msky130_fd_pr__nfet_01v8_lvt[gds]
save @m.xm14.msky130_fd_pr__nfet_01v8_lvt[gm]
save @m.xm14.msky130_fd_pr__nfet_01v8_lvt[vdsat]
save @m.xm14.msky130_fd_pr__nfet_01v8_lvt[cgg]
save @m.xm14.msky130_fd_pr__nfet_01v8_lvt[cgd]

save @m.xm16.msky130_fd_pr__nfet_01v8_lvt[vth]
save @m.xm16.msky130_fd_pr__nfet_01v8_lvt[id]
save @m.xm16.msky130_fd_pr__nfet_01v8_lvt[gds]
save @m.xm16.msky130_fd_pr__nfet_01v8_lvt[gm]
save @m.xm16.msky130_fd_pr__nfet_01v8_lvt[vdsat]
save @m.xm16.msky130_fd_pr__nfet_01v8_lvt[cgg]
save @m.xm16.msky130_fd_pr__nfet_01v8_lvt[cgd]

save @m.xm17.msky130_fd_pr__nfet_01v8_lvt[vth]
save @m.xm17.msky130_fd_pr__nfet_01v8_lvt[id]
save @m.xm17.msky130_fd_pr__nfet_01v8_lvt[gds]
save @m.xm17.msky130_fd_pr__nfet_01v8_lvt[gm]
save @m.xm17.msky130_fd_pr__nfet_01v8_lvt[vdsat]
save @m.xm17.msky130_fd_pr__nfet_01v8_lvt[cgg]
save @m.xm17.msky130_fd_pr__nfet_01v8_lvt[cgd]

save @m.xm18.msky130_fd_pr__nfet_01v8_lvt[vth]
save @m.xm18.msky130_fd_pr__nfet_01v8_lvt[id]
save @m.xm18.msky130_fd_pr__nfet_01v8_lvt[gds]
save @m.xm18.msky130_fd_pr__nfet_01v8_lvt[gm]
save @m.xm18.msky130_fd_pr__nfet_01v8_lvt[vdsat]
save @m.xm18.msky130_fd_pr__nfet_01v8_lvt[cgg]
save @m.xm18.msky130_fd_pr__nfet_01v8_lvt[cgd]

save @m.xm20.msky130_fd_pr__nfet_01v8_lvt[vth]
save @m.xm20.msky130_fd_pr__nfet_01v8_lvt[id]
save @m.xm20.msky130_fd_pr__nfet_01v8_lvt[gds]
save @m.xm20.msky130_fd_pr__nfet_01v8_lvt[gm]
save @m.xm20.msky130_fd_pr__nfet_01v8_lvt[vdsat]
save @m.xm20.msky130_fd_pr__nfet_01v8_lvt[cgg]
save @m.xm20.msky130_fd_pr__nfet_01v8_lvt[cgd]

save @m.xm22.msky130_fd_pr__nfet_01v8_lvt[vth]
save @m.xm22.msky130_fd_pr__nfet_01v8_lvt[id]
save @m.xm22.msky130_fd_pr__nfet_01v8_lvt[gds]
save @m.xm22.msky130_fd_pr__nfet_01v8_lvt[gm]
save @m.xm22.msky130_fd_pr__nfet_01v8_lvt[vdsat]
save @m.xm22.msky130_fd_pr__nfet_01v8_lvt[cgg]
save @m.xm22.msky130_fd_pr__nfet_01v8_lvt[cgd]

save @m.xm26.msky130_fd_pr__nfet_01v8_lvt[vth]
save @m.xm26.msky130_fd_pr__nfet_01v8_lvt[id]
save @m.xm26.msky130_fd_pr__nfet_01v8_lvt[gds]
save @m.xm26.msky130_fd_pr__nfet_01v8_lvt[gm]
save @m.xm26.msky130_fd_pr__nfet_01v8_lvt[vdsat]
save @m.xm26.msky130_fd_pr__nfet_01v8_lvt[cgg]
save @m.xm26.msky130_fd_pr__nfet_01v8_lvt[cgd]

save @m.xm25.msky130_fd_pr__nfet_01v8_lvt[vth]
save @m.xm25.msky130_fd_pr__nfet_01v8_lvt[id]
save @m.xm25.msky130_fd_pr__nfet_01v8_lvt[gds]
save @m.xm25.msky130_fd_pr__nfet_01v8_lvt[gm]
save @m.xm25.msky130_fd_pr__nfet_01v8_lvt[vdsat]
save @m.xm25.msky130_fd_pr__nfet_01v8_lvt[cgg]
save @m.xm25.msky130_fd_pr__nfet_01v8_lvt[cgd]

save @m.xm28.msky130_fd_pr__pfet_01v8_lvt[vth]
save @m.xm28.msky130_fd_pr__pfet_01v8_lvt[id]
save @m.xm28.msky130_fd_pr__pfet_01v8_lvt[gds]
save @m.xm28.msky130_fd_pr__pfet_01v8_lvt[gm]
save @m.xm28.msky130_fd_pr__pfet_01v8_lvt[vdsat]
save @m.xm28.msky130_fd_pr__pfet_01v8_lvt[cgg]
save @m.xm28.msky130_fd_pr__pfet_01v8_lvt[cgd]

save @m.xm4.msky130_fd_pr__pfet_01v8_lvt[vth]
save @m.xm4.msky130_fd_pr__pfet_01v8_lvt[id]
save @m.xm4.msky130_fd_pr__pfet_01v8_lvt[gds]
save @m.xm4.msky130_fd_pr__pfet_01v8_lvt[gm]
save @m.xm4.msky130_fd_pr__pfet_01v8_lvt[vdsat]
save @m.xm4.msky130_fd_pr__pfet_01v8_lvt[cgg]
save @m.xm4.msky130_fd_pr__pfet_01v8_lvt[cgd]

save @m.xm5.msky130_fd_pr__pfet_01v8_lvt[vth]
save @m.xm5.msky130_fd_pr__pfet_01v8_lvt[id]
save @m.xm5.msky130_fd_pr__pfet_01v8_lvt[gds]
save @m.xm5.msky130_fd_pr__pfet_01v8_lvt[gm]
save @m.xm5.msky130_fd_pr__pfet_01v8_lvt[vdsat]
save @m.xm5.msky130_fd_pr__pfet_01v8_lvt[cgg]
save @m.xm5.msky130_fd_pr__pfet_01v8_lvt[cgd]

save @m.xm6.msky130_fd_pr__pfet_01v8_lvt[vth]
save @m.xm6.msky130_fd_pr__pfet_01v8_lvt[id]
save @m.xm6.msky130_fd_pr__pfet_01v8_lvt[gds]
save @m.xm6.msky130_fd_pr__pfet_01v8_lvt[gm]
save @m.xm6.msky130_fd_pr__pfet_01v8_lvt[vdsat]
save @m.xm6.msky130_fd_pr__pfet_01v8_lvt[cgg]
save @m.xm6.msky130_fd_pr__pfet_01v8_lvt[cgd]

save @m.xm7.msky130_fd_pr__pfet_01v8_lvt[vth]
save @m.xm7.msky130_fd_pr__pfet_01v8_lvt[id]
save @m.xm7.msky130_fd_pr__pfet_01v8_lvt[gds]
save @m.xm7.msky130_fd_pr__pfet_01v8_lvt[gm]
save @m.xm7.msky130_fd_pr__pfet_01v8_lvt[vdsat]
save @m.xm7.msky130_fd_pr__pfet_01v8_lvt[cgg]
save @m.xm7.msky130_fd_pr__pfet_01v8_lvt[cgd]

save @m.xm12.msky130_fd_pr__pfet_01v8_lvt[vth]
save @m.xm12.msky130_fd_pr__pfet_01v8_lvt[id]
save @m.xm12.msky130_fd_pr__pfet_01v8_lvt[gds]
save @m.xm12.msky130_fd_pr__pfet_01v8_lvt[gm]
save @m.xm12.msky130_fd_pr__pfet_01v8_lvt[vdsat]
save @m.xm12.msky130_fd_pr__pfet_01v8_lvt[cgg]
save @m.xm12.msky130_fd_pr__pfet_01v8_lvt[cgd]

save @m.xm15.msky130_fd_pr__pfet_01v8_lvt[vth]
save @m.xm15.msky130_fd_pr__pfet_01v8_lvt[id]
save @m.xm15.msky130_fd_pr__pfet_01v8_lvt[gds]
save @m.xm15.msky130_fd_pr__pfet_01v8_lvt[gm]
save @m.xm15.msky130_fd_pr__pfet_01v8_lvt[vdsat]
save @m.xm15.msky130_fd_pr__pfet_01v8_lvt[cgg]
save @m.xm15.msky130_fd_pr__pfet_01v8_lvt[cgd]

save @m.xm19.msky130_fd_pr__pfet_01v8_lvt[vth]
save @m.xm19.msky130_fd_pr__pfet_01v8_lvt[id]
save @m.xm19.msky130_fd_pr__pfet_01v8_lvt[gds]
save @m.xm19.msky130_fd_pr__pfet_01v8_lvt[gm]
save @m.xm19.msky130_fd_pr__pfet_01v8_lvt[vdsat]
save @m.xm19.msky130_fd_pr__pfet_01v8_lvt[cgg]
save @m.xm19.msky130_fd_pr__pfet_01v8_lvt[cgd]

save @m.xm21.msky130_fd_pr__pfet_01v8_lvt[vth]
save @m.xm21.msky130_fd_pr__pfet_01v8_lvt[id]
save @m.xm21.msky130_fd_pr__pfet_01v8_lvt[gds]
save @m.xm21.msky130_fd_pr__pfet_01v8_lvt[gm]
save @m.xm21.msky130_fd_pr__pfet_01v8_lvt[vdsat]
save @m.xm21.msky130_fd_pr__pfet_01v8_lvt[cgg]
save @m.xm21.msky130_fd_pr__pfet_01v8_lvt[cgd]

*tran 1n 2u
*op
ac dec 100 1 100T
setplot new
let frequency = ac.frequency
let T = ac.voutp-ac.voutn
let T_mag = db(T)
let T_ph  = cph(T)*180/pi

let T1 = ac.voutpc
let PSRR = T/T1
let PSRR_mag = db(PSRR)
let PSRR_ph  = cph(PSRR)*180/pi
let T1_mag = db(T1)
let T1_ph  = cph(T1)*180/pi
*let T2 = (ac.outp-ac.outn)/(ac.outp1-ac.outn1)
*let T2_mag = db(T2)
*let T2_ph  = cph(T2)*180/pi
plot T_mag T_ph xlog
plot T1_mag T1_ph xlog
plot PSRR_mag PSRR_ph xlog
write P_in_folded_cascode.raw
.endc

**** end user architecture code
**.ends
.end
